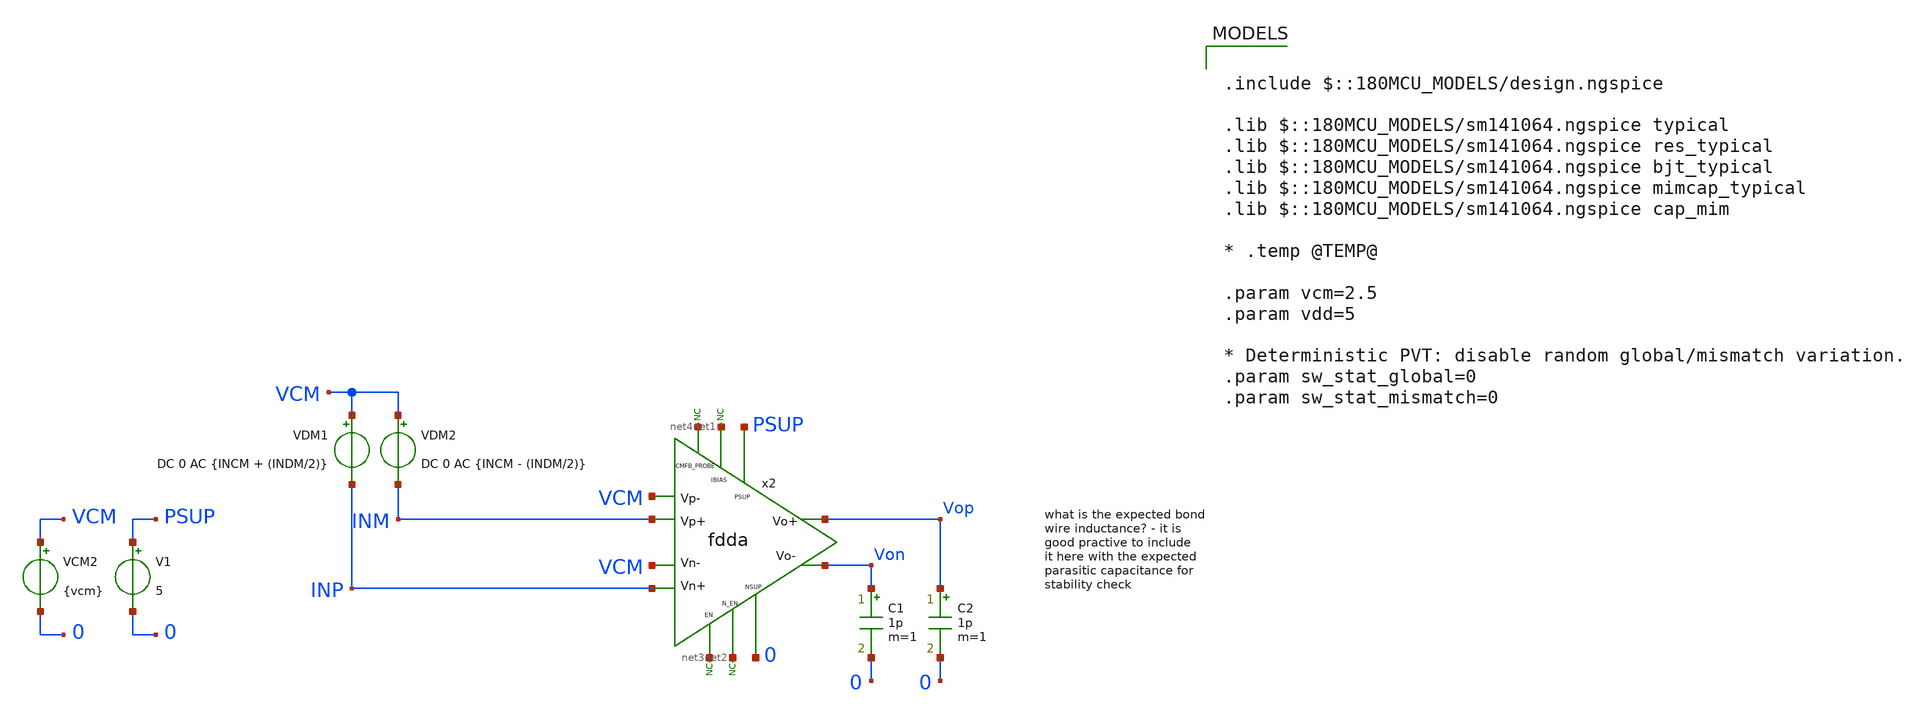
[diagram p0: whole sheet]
** sch_path: xschem/blocks/fdda/tb_fdda_cmrr.sch
**.subckt tb_fdda_cmrr
C1 Von 0 1p m=1
x2 PSUP VCM VCM INP INM Vop Von net1 net2 net3 0 net4 fdda
* noconn #net1
* noconn #net3
* noconn #net2
V1 PSUP 0 5
C2 Vop 0 1p m=1
VCM2 VCM 0 {vcm}
VDM2 VCM INM DC 0 AC {INCM - (INDM/2)}
VDM1 VCM INP DC 0 AC {INCM + (INDM/2)}
* noconn #net4
**** begin user architecture code

.include $::180MCU_MODELS/design.ngspice

.lib $::180MCU_MODELS/sm141064.ngspice typical
.lib $::180MCU_MODELS/sm141064.ngspice res_typical
.lib $::180MCU_MODELS/sm141064.ngspice bjt_typical
.lib $::180MCU_MODELS/sm141064.ngspice mimcap_typical
.lib $::180MCU_MODELS/sm141064.ngspice cap_mim

* .temp @TEMP@

.param vcm=2.5
.param vdd=5

* Deterministic PVT: disable random global/mismatch variation.
.param sw_stat_global=0
.param sw_stat_mismatch=0



.control
set units=degrees
save all

.param INCM=0
.param INDM=1

* ==================================================
* 1. Differential gain
* ==================================================

alterparam INCM=0
alterparam INDM=1
reset

ac dec 100 1 1G

let Vdi = v(INP) - v(INM)
let Vdo = v(Vop) - v(Von)
let Ad = Vdo / Vdi
let gain_diff_db = db(Ad)
let phase_diff_deg = cph(Ad)

meas ac UGF when gain_diff_db=0
meas ac phase_margin find phase_diff_deg when gain_diff_db=0

write tb_fdda_aol.raw frequency v(Vop) v(Von) Vdo Ad gain_diff_db phase_diff_deg

* ==================================================
* 2. Common-mode gain
* ==================================================

alterparam INCM=1
alterparam INDM=0
reset

ac dec 100 1 1G

let Vci = (v(INP) + v(INM))/2
let Vco = v(Vop) - v(Von)
let Ac  = Vco/Vci

let gain_comm_db = db(Ac)
let phase_comm_deg = cph(Ac)

write tb_fdda_acm.raw frequency v(Vop) v(Von) Vco Ac gain_comm_db phase_comm_deg

* ==================================================
* 3. CMRR
* ==================================================

.endc


**** end user architecture code
**.ends

* expanding   symbol:  blocks/fdda/fdda.sym # of pins=12
** sym_path: xschem/blocks/fdda/fdda.sym
** sch_path: xschem/blocks/fdda/fdda.sch
.subckt fdda PSUP Vp- Vn+ Vn- Vp+ Vo+ Vo- IBIAS N_EN EN NSUP CMFB_PROBE
*.ipin PSUP
*.ipin NSUP
*.ipin N_EN
*.ipin EN
*.ipin IBIAS
*.ipin Vp+
*.ipin Vp-
*.ipin Vn+
*.ipin Vn-
*.opin Vo+
*.opin Vo-
*.ipin CMFB_PROBE
* noconn N_EN
* noconn EN
I0 vb4 vb2 1u
XM7 vb1 vb1 PSUP PSUP pfet_06v0 L=4u W=2u nf=1 ad='int((nf+1)/2) * W/nf * 0.18u' as='int((nf+2)/2) * W/nf * 0.18u'
+ pd='2*int((nf+1)/2) * (W/nf + 0.18u)' ps='2*int((nf+2)/2) * (W/nf + 0.18u)' nrd='0.18u / W' nrs='0.18u / W'
+ sa=0 sb=0 sd=0 m=4
* noconn IBIAS
XM16 vb3 vb3 NSUP NSUP nfet_06v0 L=4u W=2u nf=1 ad='int((nf+1)/2) * W/nf * 0.18u' as='int((nf+2)/2) * W/nf * 0.18u'
+ pd='2*int((nf+1)/2) * (W/nf + 0.18u)' ps='2*int((nf+2)/2) * (W/nf + 0.18u)' nrd='0.18u / W' nrs='0.18u / W'
+ sa=0 sb=0 sd=0 m=4
XM9 sum_n Vp- n1 PSUP pfet_06v0 L=2u W=4u nf=5 ad='int((nf+1)/2) * W/nf * 0.18u' as='int((nf+2)/2) * W/nf * 0.18u'
+ pd='2*int((nf+1)/2) * (W/nf + 0.18u)' ps='2*int((nf+2)/2) * (W/nf + 0.18u)' nrd='0.18u / W' nrs='0.18u / W'
+ sa=0 sb=0 sd=0 m=10
XM1 sum_p Vp+ n1 PSUP pfet_06v0 L=2u W=4u nf=5 ad='int((nf+1)/2) * W/nf * 0.18u' as='int((nf+2)/2) * W/nf * 0.18u'
+ pd='2*int((nf+1)/2) * (W/nf + 0.18u)' ps='2*int((nf+2)/2) * (W/nf + 0.18u)' nrd='0.18u / W' nrs='0.18u / W'
+ sa=0 sb=0 sd=0 m=10
XM2 n1 vb1 PSUP PSUP pfet_06v0 L=4u W=2u nf=1 ad='int((nf+1)/2) * W/nf * 0.18u' as='int((nf+2)/2) * W/nf * 0.18u'
+ pd='2*int((nf+1)/2) * (W/nf + 0.18u)' ps='2*int((nf+2)/2) * (W/nf + 0.18u)' nrd='0.18u / W' nrs='0.18u / W'
+ sa=0 sb=0 sd=0 m=4
XM6 n2 vb1 PSUP PSUP pfet_06v0 L=4u W=2u nf=1 ad='int((nf+1)/2) * W/nf * 0.18u' as='int((nf+2)/2) * W/nf * 0.18u'
+ pd='2*int((nf+1)/2) * (W/nf + 0.18u)' ps='2*int((nf+2)/2) * (W/nf + 0.18u)' nrd='0.18u / W' nrs='0.18u / W'
+ sa=0 sb=0 sd=0 m=4
XM24 sum_p Vn+ n2 PSUP pfet_06v0 L=2u W=4u nf=5 ad='int((nf+1)/2) * W/nf * 0.18u' as='int((nf+2)/2) * W/nf * 0.18u'
+ pd='2*int((nf+1)/2) * (W/nf + 0.18u)' ps='2*int((nf+2)/2) * (W/nf + 0.18u)' nrd='0.18u / W' nrs='0.18u / W'
+ sa=0 sb=0 sd=0 m=10
XM13 sum_n Vn- n2 PSUP pfet_06v0 L=2u W=4u nf=5 ad='int((nf+1)/2) * W/nf * 0.18u' as='int((nf+2)/2) * W/nf * 0.18u'
+ pd='2*int((nf+1)/2) * (W/nf + 0.18u)' ps='2*int((nf+2)/2) * (W/nf + 0.18u)' nrd='0.18u / W' nrs='0.18u / W'
+ sa=0 sb=0 sd=0 m=10
XM12 Vo- vb4 n6 PSUP pfet_06v0 L=2u W=4u nf=5 ad='int((nf+1)/2) * W/nf * 0.18u' as='int((nf+2)/2) * W/nf * 0.18u'
+ pd='2*int((nf+1)/2) * (W/nf + 0.18u)' ps='2*int((nf+2)/2) * (W/nf + 0.18u)' nrd='0.18u / W' nrs='0.18u / W'
+ sa=0 sb=0 sd=0 m=8
XM15 Vo+ vb4 n7 PSUP pfet_06v0 L=2u W=4u nf=5 ad='int((nf+1)/2) * W/nf * 0.18u' as='int((nf+2)/2) * W/nf * 0.18u'
+ pd='2*int((nf+1)/2) * (W/nf + 0.18u)' ps='2*int((nf+2)/2) * (W/nf + 0.18u)' nrd='0.18u / W' nrs='0.18u / W'
+ sa=0 sb=0 sd=0 m=8
XM19 n6 Vcmfb PSUP PSUP pfet_06v0 L=8u W=2u nf=1 ad='int((nf+1)/2) * W/nf * 0.18u' as='int((nf+2)/2) * W/nf * 0.18u'
+ pd='2*int((nf+1)/2) * (W/nf + 0.18u)' ps='2*int((nf+2)/2) * (W/nf + 0.18u)' nrd='0.18u / W' nrs='0.18u / W'
+ sa=0 sb=0 sd=0 m=8
XM20 n7 Vcmfb PSUP PSUP pfet_06v0 L=8u W=2u nf=1 ad='int((nf+1)/2) * W/nf * 0.18u' as='int((nf+2)/2) * W/nf * 0.18u'
+ pd='2*int((nf+1)/2) * (W/nf + 0.18u)' ps='2*int((nf+2)/2) * (W/nf + 0.18u)' nrd='0.18u / W' nrs='0.18u / W'
+ sa=0 sb=0 sd=0 m=8
XM26 sum_n vb3 NSUP NSUP nfet_06v0 L=4u W=2u nf=1 ad='int((nf+1)/2) * W/nf * 0.18u' as='int((nf+2)/2) * W/nf * 0.18u'
+ pd='2*int((nf+1)/2) * (W/nf + 0.18u)' ps='2*int((nf+2)/2) * (W/nf + 0.18u)' nrd='0.18u / W' nrs='0.18u / W'
+ sa=0 sb=0 sd=0 m=8
XM27 sum_p vb3 NSUP NSUP nfet_06v0 L=4u W=2u nf=1 ad='int((nf+1)/2) * W/nf * 0.18u' as='int((nf+2)/2) * W/nf * 0.18u'
+ pd='2*int((nf+1)/2) * (W/nf + 0.18u)' ps='2*int((nf+2)/2) * (W/nf + 0.18u)' nrd='0.18u / W' nrs='0.18u / W'
+ sa=0 sb=0 sd=0 m=8
XM28 Vo+ vb2 sum_n NSUP nfet_06v0 L=2u W=4u nf=5 ad='int((nf+1)/2) * W/nf * 0.18u' as='int((nf+2)/2) * W/nf * 0.18u'
+ pd='2*int((nf+1)/2) * (W/nf + 0.18u)' ps='2*int((nf+2)/2) * (W/nf + 0.18u)' nrd='0.18u / W' nrs='0.18u / W'
+ sa=0 sb=0 sd=0 m=4
XM29 Vo- vb2 sum_p NSUP nfet_06v0 L=2u W=4u nf=5 ad='int((nf+1)/2) * W/nf * 0.18u' as='int((nf+2)/2) * W/nf * 0.18u'
+ pd='2*int((nf+1)/2) * (W/nf + 0.18u)' ps='2*int((nf+2)/2) * (W/nf + 0.18u)' nrd='0.18u / W' nrs='0.18u / W'
+ sa=0 sb=0 sd=0 m=4
XM30 vb2 vb2 vb3 NSUP nfet_06v0 L=4u W=2u nf=1 ad='int((nf+1)/2) * W/nf * 0.18u' as='int((nf+2)/2) * W/nf * 0.18u'
+ pd='2*int((nf+1)/2) * (W/nf + 0.18u)' ps='2*int((nf+2)/2) * (W/nf + 0.18u)' nrd='0.18u / W' nrs='0.18u / W'
+ sa=0 sb=0 sd=0 m=4
XM31 vb4 vb4 vb1 PSUP pfet_06v0 L=4u W=2u nf=1 ad='int((nf+1)/2) * W/nf * 0.18u' as='int((nf+2)/2) * W/nf * 0.18u'
+ pd='2*int((nf+1)/2) * (W/nf + 0.18u)' ps='2*int((nf+2)/2) * (W/nf + 0.18u)' nrd='0.18u / W' nrs='0.18u / W'
+ sa=0 sb=0 sd=0 m=4
XM3 Vcmfb Vcmfb PSUP PSUP pfet_06v0 L=8u W=2u nf=1 ad='int((nf+1)/2) * W/nf * 0.18u' as='int((nf+2)/2) * W/nf * 0.18u'
+ pd='2*int((nf+1)/2) * (W/nf + 0.18u)' ps='2*int((nf+2)/2) * (W/nf + 0.18u)' nrd='0.18u / W' nrs='0.18u / W'
+ sa=0 sb=0 sd=0 m=2
XM8 net1 net1 PSUP PSUP pfet_06v0 L=8u W=2u nf=1 ad='int((nf+1)/2) * W/nf * 0.18u' as='int((nf+2)/2) * W/nf * 0.18u'
+ pd='2*int((nf+1)/2) * (W/nf + 0.18u)' ps='2*int((nf+2)/2) * (W/nf + 0.18u)' nrd='0.18u / W' nrs='0.18u / W'
+ sa=0 sb=0 sd=0 m=2
XM21 net1 Vcm CMFB_PROBE NSUP nfet_06v0 L=2u W=4u nf=5 ad='int((nf+1)/2) * W/nf * 0.18u' as='int((nf+2)/2) * W/nf * 0.18u'
+ pd='2*int((nf+1)/2) * (W/nf + 0.18u)' ps='2*int((nf+2)/2) * (W/nf + 0.18u)' nrd='0.18u / W' nrs='0.18u / W'
+ sa=0 sb=0 sd=0 m=4
XM25 Vcmfb Vref CMFB_PROBE NSUP nfet_06v0 L=2u W=4u nf=5 ad='int((nf+1)/2) * W/nf * 0.18u' as='int((nf+2)/2) * W/nf * 0.18u'
+ pd='2*int((nf+1)/2) * (W/nf + 0.18u)' ps='2*int((nf+2)/2) * (W/nf + 0.18u)' nrd='0.18u / W' nrs='0.18u / W'
+ sa=0 sb=0 sd=0 m=4
XM4 CMFB_PROBE vb3 NSUP NSUP nfet_06v0 L=4u W=2u nf=1 ad='int((nf+1)/2) * W/nf * 0.18u' as='int((nf+2)/2) * W/nf * 0.18u'
+ pd='2*int((nf+1)/2) * (W/nf + 0.18u)' ps='2*int((nf+2)/2) * (W/nf + 0.18u)' nrd='0.18u / W' nrs='0.18u / W'
+ sa=0 sb=0 sd=0 m=4
XM22 NSUP Vo- n5 PSUP pfet_06v0 L=2u W=4u nf=5 ad='int((nf+1)/2) * W/nf * 0.18u' as='int((nf+2)/2) * W/nf * 0.18u'
+ pd='2*int((nf+1)/2) * (W/nf + 0.18u)' ps='2*int((nf+2)/2) * (W/nf + 0.18u)' nrd='0.18u / W' nrs='0.18u / W'
+ sa=0 sb=0 sd=0 m=4
XM23 NSUP Vo+ n4 PSUP pfet_06v0 L=2u W=4u nf=5 ad='int((nf+1)/2) * W/nf * 0.18u' as='int((nf+2)/2) * W/nf * 0.18u'
+ pd='2*int((nf+1)/2) * (W/nf + 0.18u)' ps='2*int((nf+2)/2) * (W/nf + 0.18u)' nrd='0.18u / W' nrs='0.18u / W'
+ sa=0 sb=0 sd=0 m=4
XR1 n4 Vcm NSUP ppolyf_u_3k r_width=1e-6 r_length=1000e-6 m=1
XR2 Vcm n5 NSUP ppolyf_u_3k r_width=1e-6 r_length=1000e-6 m=1
XM5 n4 vb1 PSUP PSUP pfet_06v0 L=4u W=2u nf=1 ad='int((nf+1)/2) * W/nf * 0.18u' as='int((nf+2)/2) * W/nf * 0.18u'
+ pd='2*int((nf+1)/2) * (W/nf + 0.18u)' ps='2*int((nf+2)/2) * (W/nf + 0.18u)' nrd='0.18u / W' nrs='0.18u / W'
+ sa=0 sb=0 sd=0 m=4
XM17 n5 vb1 PSUP PSUP pfet_06v0 L=4u W=2u nf=1 ad='int((nf+1)/2) * W/nf * 0.18u' as='int((nf+2)/2) * W/nf * 0.18u'
+ pd='2*int((nf+1)/2) * (W/nf + 0.18u)' ps='2*int((nf+2)/2) * (W/nf + 0.18u)' nrd='0.18u / W' nrs='0.18u / W'
+ sa=0 sb=0 sd=0 m=4
R3 vb1 Vref 1 m=1
.ends

.end
